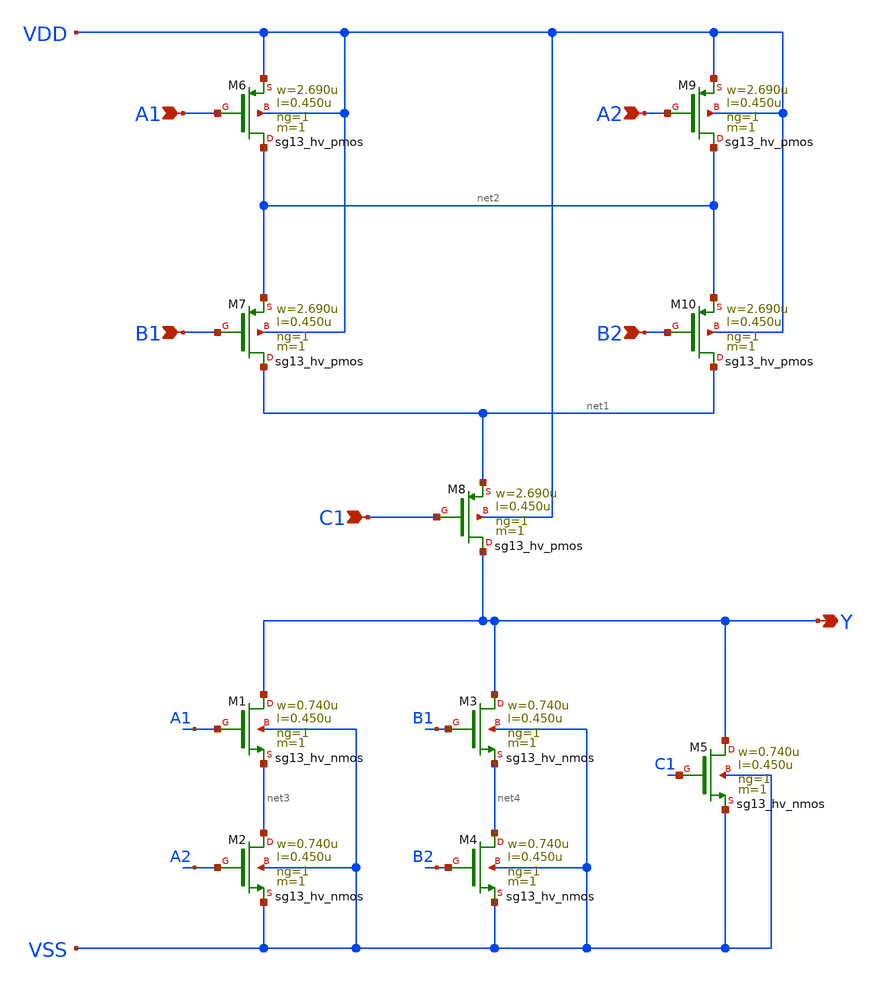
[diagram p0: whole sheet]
** sch_path: ihp-sg13g2/libs.ref/sg13g2_stdcell_hv/sch/xschem/sg13g2_hv_a221oi_1.sch
* Copyright 2023 IHP PDK Authors
* Licensed under the Apache License, Version 2.0 (the "License");
* you may not use this file except in compliance with the License.
* You may obtain a copy of the License at
* https://www.apache.org/licenses/LICENSE-2.0
* Unless required by applicable law or agreed to in writing, software
* distributed under the License is distributed on an "AS IS" BASIS,
* WITHOUT WARRANTIES OR CONDITIONS OF ANY KIND, either express or implied.
* See the License for the specific language governing permissions and
* limitations under the License.
**.subckt sg13g2_hv_a221oi_1 A1 A2 B1 Y B2 C1
*.ipin A1
*.ipin A2
*.ipin B1
*.opin Y
*.ipin B2
*.ipin C1
XM1 Y A1 net3 VSS sg13_hv_nmos w=0.740u l=0.450u ng=1 m=1 mm_ok=1
XM2 net3 A2 VSS VSS sg13_hv_nmos w=0.740u l=0.450u ng=1 m=1 mm_ok=1
XM3 Y B1 net4 VSS sg13_hv_nmos w=0.740u l=0.450u ng=1 m=1 mm_ok=1
XM4 net4 B2 VSS VSS sg13_hv_nmos w=0.740u l=0.450u ng=1 m=1 mm_ok=1
XM5 Y C1 VSS VSS sg13_hv_nmos w=0.740u l=0.450u ng=1 m=1 mm_ok=1
XM6 net2 A1 VDD VDD sg13_hv_pmos w=2.690u l=0.450u ng=1 m=1 mm_ok=1
XM7 net1 B1 net2 VDD sg13_hv_pmos w=2.690u l=0.450u ng=1 m=1 mm_ok=1
XM8 Y C1 net1 VDD sg13_hv_pmos w=2.690u l=0.450u ng=1 m=1 mm_ok=1
XM9 net2 A2 VDD VDD sg13_hv_pmos w=2.690u l=0.450u ng=1 m=1 mm_ok=1
XM10 net1 B2 net2 VDD sg13_hv_pmos w=2.690u l=0.450u ng=1 m=1 mm_ok=1
**.ends
.end
